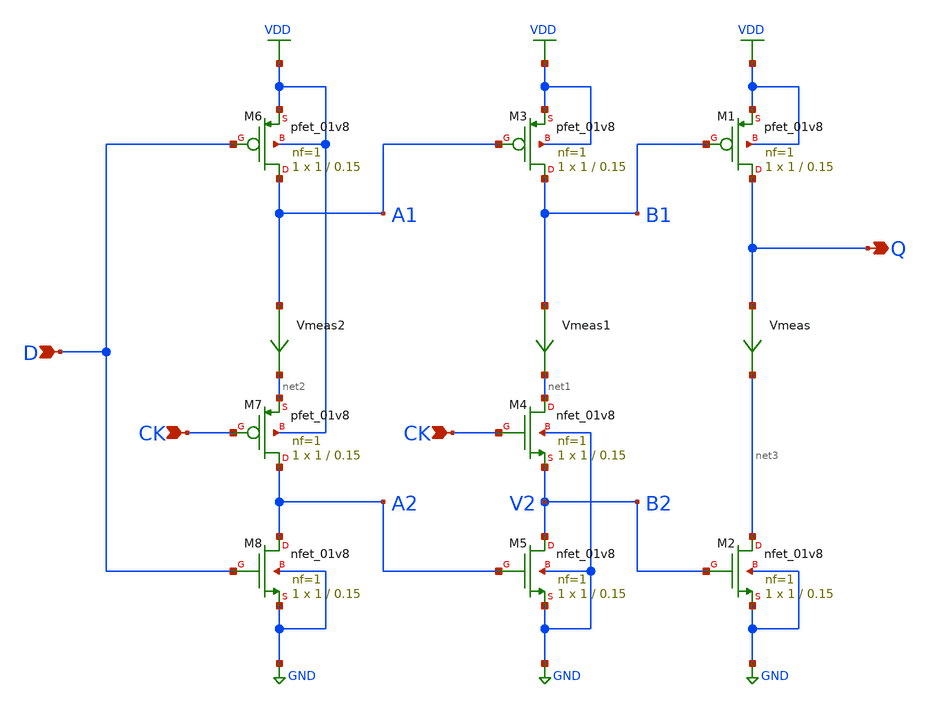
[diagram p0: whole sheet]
** sch_path: projects/pll/divider/xschem_ngspice/TSPC_FF.sch
**.subckt TSPC_FF CK CK D Q
*.ipin CK
*.ipin CK
*.ipin D
*.opin Q
XM1 Q B1 VDD VDD sky130_fd_pr__pfet_01v8 L=0.15 W=1 nf=1 ad='int((nf+1)/2) * W/nf * 0.29' as='int((nf+2)/2) * W/nf * 0.29'
+ pd='2*int((nf+1)/2) * (W/nf + 0.29)' ps='2*int((nf+2)/2) * (W/nf + 0.29)' nrd='0.29 / W' nrs='0.29 / W'
+ sa=0 sb=0 sd=0 mult=1 m=1
XM4 net1 CK V2 GND sky130_fd_pr__nfet_01v8 L=0.15 W=1 nf=1 ad='int((nf+1)/2) * W/nf * 0.29' as='int((nf+2)/2) * W/nf * 0.29'
+ pd='2*int((nf+1)/2) * (W/nf + 0.29)' ps='2*int((nf+2)/2) * (W/nf + 0.29)' nrd='0.29 / W' nrs='0.29 / W'
+ sa=0 sb=0 sd=0 mult=1 m=1
Vmeas Q net3 0
.save i(vmeas)
XM2 net3 V2 GND GND sky130_fd_pr__nfet_01v8 L=0.15 W=1 nf=1 ad='int((nf+1)/2) * W/nf * 0.29' as='int((nf+2)/2) * W/nf * 0.29'
+ pd='2*int((nf+1)/2) * (W/nf + 0.29)' ps='2*int((nf+2)/2) * (W/nf + 0.29)' nrd='0.29 / W' nrs='0.29 / W'
+ sa=0 sb=0 sd=0 mult=1 m=1
XM3 B1 A1 VDD VDD sky130_fd_pr__pfet_01v8 L=0.15 W=1 nf=1 ad='int((nf+1)/2) * W/nf * 0.29' as='int((nf+2)/2) * W/nf * 0.29'
+ pd='2*int((nf+1)/2) * (W/nf + 0.29)' ps='2*int((nf+2)/2) * (W/nf + 0.29)' nrd='0.29 / W' nrs='0.29 / W'
+ sa=0 sb=0 sd=0 mult=1 m=1
XM5 V2 A2 GND GND sky130_fd_pr__nfet_01v8 L=0.15 W=1 nf=1 ad='int((nf+1)/2) * W/nf * 0.29' as='int((nf+2)/2) * W/nf * 0.29'
+ pd='2*int((nf+1)/2) * (W/nf + 0.29)' ps='2*int((nf+2)/2) * (W/nf + 0.29)' nrd='0.29 / W' nrs='0.29 / W'
+ sa=0 sb=0 sd=0 mult=1 m=1
Vmeas1 B1 net1 0
.save i(vmeas1)
XM6 A1 D VDD VDD sky130_fd_pr__pfet_01v8 L=0.15 W=1 nf=1 ad='int((nf+1)/2) * W/nf * 0.29' as='int((nf+2)/2) * W/nf * 0.29'
+ pd='2*int((nf+1)/2) * (W/nf + 0.29)' ps='2*int((nf+2)/2) * (W/nf + 0.29)' nrd='0.29 / W' nrs='0.29 / W'
+ sa=0 sb=0 sd=0 mult=1 m=1
XM8 A2 D GND GND sky130_fd_pr__nfet_01v8 L=0.15 W=1 nf=1 ad='int((nf+1)/2) * W/nf * 0.29' as='int((nf+2)/2) * W/nf * 0.29'
+ pd='2*int((nf+1)/2) * (W/nf + 0.29)' ps='2*int((nf+2)/2) * (W/nf + 0.29)' nrd='0.29 / W' nrs='0.29 / W'
+ sa=0 sb=0 sd=0 mult=1 m=1
Vmeas2 A1 net2 0
.save i(vmeas2)
XM7 A2 CK net2 VDD sky130_fd_pr__pfet_01v8 L=0.15 W=1 nf=1 ad='int((nf+1)/2) * W/nf * 0.29' as='int((nf+2)/2) * W/nf * 0.29'
+ pd='2*int((nf+1)/2) * (W/nf + 0.29)' ps='2*int((nf+2)/2) * (W/nf + 0.29)' nrd='0.29 / W' nrs='0.29 / W'
+ sa=0 sb=0 sd=0 mult=1 m=1
**.ends
.GLOBAL VDD
.GLOBAL GND
.end
